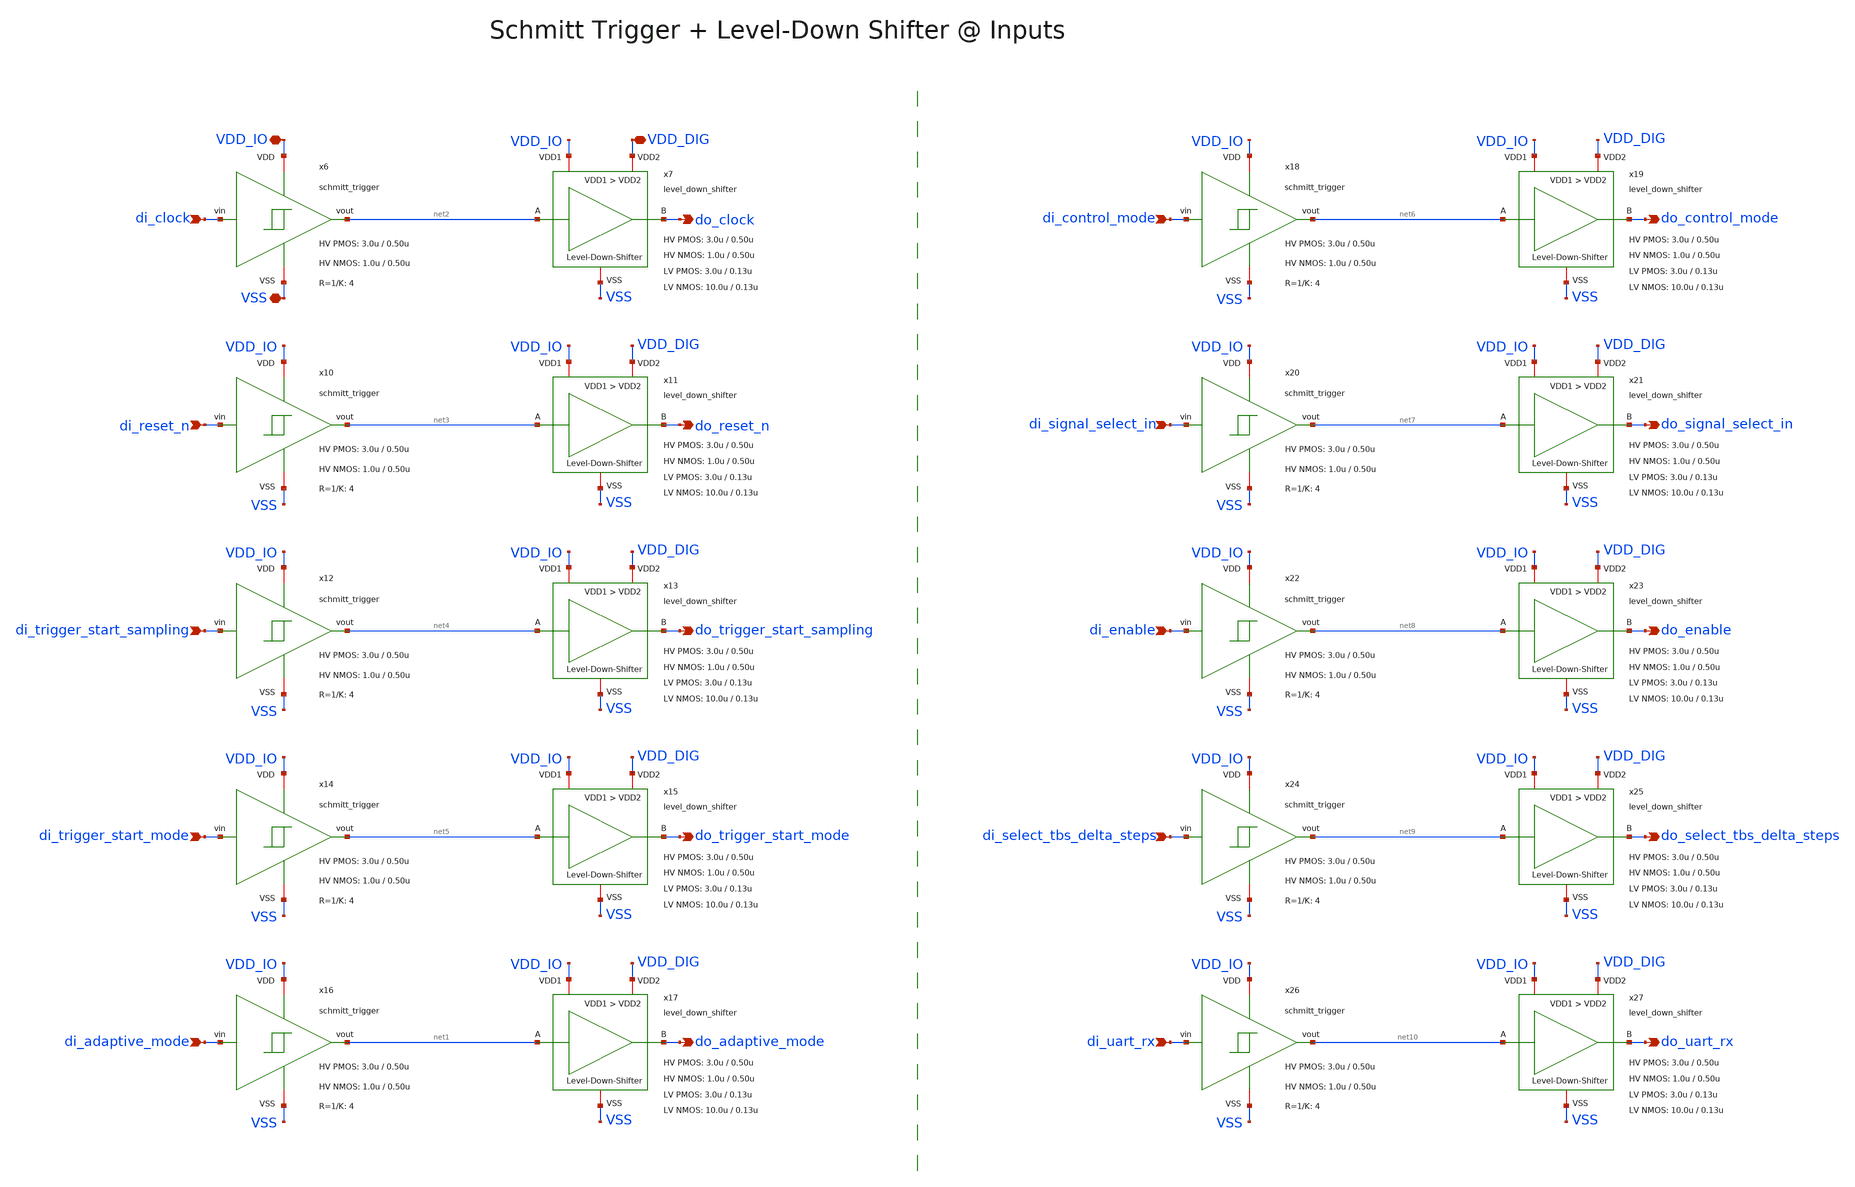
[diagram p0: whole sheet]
** sch_path: SG13G2_ATBS-ADC-main/xschem/top_level/auxiliary/input_hardware.sch
**.subckt input_hardware di_clock di_reset_n di_uart_rx di_trigger_start_sampling
*+ di_trigger_start_mode di_adaptive_mode di_control_mode di_signal_select_in di_enable di_select_tbs_delta_steps do_clock
*+ VDD_IO VDD_DIG do_trigger_start_sampling do_control_mode do_enable do_reset_n do_trigger_start_mode
*+ do_adaptive_mode do_signal_select_in do_select_tbs_delta_steps do_uart_rx VSS
*.ipin di_clock
*.ipin di_reset_n
*.ipin di_uart_rx
*.ipin di_trigger_start_sampling
*.ipin di_trigger_start_mode
*.ipin di_adaptive_mode
*.ipin di_control_mode
*.ipin di_signal_select_in
*.ipin di_enable
*.ipin di_select_tbs_delta_steps
*.opin do_clock
*.iopin VDD_IO
*.iopin VDD_DIG
*.opin do_trigger_start_sampling
*.opin do_control_mode
*.opin do_enable
*.opin do_reset_n
*.opin do_trigger_start_mode
*.opin do_adaptive_mode
*.opin do_signal_select_in
*.opin do_select_tbs_delta_steps
*.opin do_uart_rx
*.iopin VSS
x6 VDD_IO net2 di_clock VSS schmitt_trigger W_P_ST=3.0u L_P_ST=0.50u W_N_ST=1.0u L_N_ST=0.50u R=4
x7 VDD_DIG net2 do_clock VSS VDD_IO level_down_shifter W_P_HV=3.0u L_P_HV=0.50u W_N_HV=1.0u
+ L_N_HV=0.50u W_P_LV=3.0u L_P_LV=0.13u W_N_LV=10.0u L_N_LV=0.13u
x10 VDD_IO net3 di_reset_n VSS schmitt_trigger W_P_ST=3.0u L_P_ST=0.50u W_N_ST=1.0u L_N_ST=0.50u R=4
x11 VDD_DIG net3 do_reset_n VSS VDD_IO level_down_shifter W_P_HV=3.0u L_P_HV=0.50u W_N_HV=1.0u
+ L_N_HV=0.50u W_P_LV=3.0u L_P_LV=0.13u W_N_LV=10.0u L_N_LV=0.13u
x12 VDD_IO net4 di_trigger_start_sampling VSS schmitt_trigger W_P_ST=3.0u L_P_ST=0.50u W_N_ST=1.0u
+ L_N_ST=0.50u R=4
x13 VDD_DIG net4 do_trigger_start_sampling VSS VDD_IO level_down_shifter W_P_HV=3.0u L_P_HV=0.50u
+ W_N_HV=1.0u L_N_HV=0.50u W_P_LV=3.0u L_P_LV=0.13u W_N_LV=10.0u L_N_LV=0.13u
x14 VDD_IO net5 di_trigger_start_mode VSS schmitt_trigger W_P_ST=3.0u L_P_ST=0.50u W_N_ST=1.0u
+ L_N_ST=0.50u R=4
x15 VDD_DIG net5 do_trigger_start_mode VSS VDD_IO level_down_shifter W_P_HV=3.0u L_P_HV=0.50u
+ W_N_HV=1.0u L_N_HV=0.50u W_P_LV=3.0u L_P_LV=0.13u W_N_LV=10.0u L_N_LV=0.13u
x16 VDD_IO net1 di_adaptive_mode VSS schmitt_trigger W_P_ST=3.0u L_P_ST=0.50u W_N_ST=1.0u
+ L_N_ST=0.50u R=4
x17 VDD_DIG net1 do_adaptive_mode VSS VDD_IO level_down_shifter W_P_HV=3.0u L_P_HV=0.50u W_N_HV=1.0u
+ L_N_HV=0.50u W_P_LV=3.0u L_P_LV=0.13u W_N_LV=10.0u L_N_LV=0.13u
x18 VDD_IO net6 di_control_mode VSS schmitt_trigger W_P_ST=3.0u L_P_ST=0.50u W_N_ST=1.0u
+ L_N_ST=0.50u R=4
x19 VDD_DIG net6 do_control_mode VSS VDD_IO level_down_shifter W_P_HV=3.0u L_P_HV=0.50u W_N_HV=1.0u
+ L_N_HV=0.50u W_P_LV=3.0u L_P_LV=0.13u W_N_LV=10.0u L_N_LV=0.13u
x20 VDD_IO net7 di_signal_select_in VSS schmitt_trigger W_P_ST=3.0u L_P_ST=0.50u W_N_ST=1.0u
+ L_N_ST=0.50u R=4
x21 VDD_DIG net7 do_signal_select_in VSS VDD_IO level_down_shifter W_P_HV=3.0u L_P_HV=0.50u
+ W_N_HV=1.0u L_N_HV=0.50u W_P_LV=3.0u L_P_LV=0.13u W_N_LV=10.0u L_N_LV=0.13u
x22 VDD_IO net8 di_enable VSS schmitt_trigger W_P_ST=3.0u L_P_ST=0.50u W_N_ST=1.0u L_N_ST=0.50u R=4
x23 VDD_DIG net8 do_enable VSS VDD_IO level_down_shifter W_P_HV=3.0u L_P_HV=0.50u W_N_HV=1.0u
+ L_N_HV=0.50u W_P_LV=3.0u L_P_LV=0.13u W_N_LV=10.0u L_N_LV=0.13u
x24 VDD_IO net9 di_select_tbs_delta_steps VSS schmitt_trigger W_P_ST=3.0u L_P_ST=0.50u W_N_ST=1.0u
+ L_N_ST=0.50u R=4
x25 VDD_DIG net9 do_select_tbs_delta_steps VSS VDD_IO level_down_shifter W_P_HV=3.0u L_P_HV=0.50u
+ W_N_HV=1.0u L_N_HV=0.50u W_P_LV=3.0u L_P_LV=0.13u W_N_LV=10.0u L_N_LV=0.13u
x26 VDD_IO net10 di_uart_rx VSS schmitt_trigger W_P_ST=3.0u L_P_ST=0.50u W_N_ST=1.0u L_N_ST=0.50u
+ R=4
x27 VDD_DIG net10 do_uart_rx VSS VDD_IO level_down_shifter W_P_HV=3.0u L_P_HV=0.50u W_N_HV=1.0u
+ L_N_HV=0.50u W_P_LV=3.0u L_P_LV=0.13u W_N_LV=10.0u L_N_LV=0.13u
**.ends

* expanding   symbol:  schmitt_trigger/schmitt_trigger.sym # of pins=4
** sym_path: SG13G2_ATBS-ADC-main/xschem/schmitt_trigger/schmitt_trigger.sym
** sch_path: SG13G2_ATBS-ADC-main/xschem/schmitt_trigger/schmitt_trigger.sch
.subckt schmitt_trigger VDD vout vin VSS  W_P_ST=3.0u L_P_ST=0.50u W_N_ST=1.0u L_N_ST=0.50u R=4
*.iopin VDD
*.opin vout
*.iopin VSS
*.ipin vin
x1 VDD net2 vout VSS inverter_hv W_P=W_P_ST L_P=L_P_ST W_N=W_N_ST L_N=L_N_ST
XM5 net3 vin VDD VDD sg13_hv_pmos w=W_P_ST l=L_P_ST ng=1 m=1 mm_ok=1
XM4 net2 vin net3 VDD sg13_hv_pmos w=W_P_ST l=L_P_ST ng=1 m=1 mm_ok=1
XM6 VSS net2 net3 VDD sg13_hv_pmos w=R*W_P_ST l=L_P_ST ng=1 m=1 mm_ok=1
XM1 net1 vin VSS VSS sg13_hv_nmos w=W_N_ST l=L_N_ST ng=1 m=1 mm_ok=1
XM2 net2 vin net1 VSS sg13_hv_nmos w=W_N_ST l=L_N_ST ng=1 m=1 mm_ok=1
XM3 VDD net2 net1 VSS sg13_hv_nmos w=R*W_N_ST l=L_N_ST ng=1 m=1 mm_ok=1
.ends


* expanding   symbol:  level_shifter/level_down_shifter.sym # of pins=5
** sym_path: SG13G2_ATBS-ADC-main/xschem/level_shifter/level_down_shifter.sym
** sch_path: SG13G2_ATBS-ADC-main/xschem/level_shifter/level_down_shifter.sch
.subckt level_down_shifter VDD2 A B VSS VDD1  W_P_HV=3.0u L_P_HV=0.50u W_N_HV=1.0u L_N_HV=0.50u
+ W_P_LV=3.0u L_P_LV=0.13u W_N_LV=10.0u L_N_LV=0.13u
*.ipin A
*.iopin VDD1
*.iopin VSS
*.opin B
*.iopin VDD2
x3 VDD2 T B VSS inverter_lv W_P=W_P_LV L_P=L_P_LV W_N=0.1*W_N_LV L_N=L_N_LV
x1 VDD1 A A! VSS inverter_hv W_P=W_P_HV L_P=L_P_HV W_N=W_N_HV L_N=L_N_HV
x2 VDD1 A! net2 VSS inverter_hv W_P=W_P_HV L_P=L_P_HV W_N=W_N_HV L_N=L_N_HV
XM1 net1 A! VSS VSS sg13_lv_nmos w=W_N_LV l=L_N_LV ng=1 m=1 mm_ok=1
XM3 net1 T VDD2 VDD2 sg13_lv_pmos w=W_P_LV l=L_P_LV ng=1 m=1 mm_ok=1
XM2 T net2 VSS VSS sg13_lv_nmos w=W_N_LV l=L_N_LV ng=1 m=1 mm_ok=1
XM4 T net1 VDD2 VDD2 sg13_lv_pmos w=W_P_LV l=L_P_LV ng=1 m=1 mm_ok=1
.ends


* expanding   symbol:  inverter/inverter_hv.sym # of pins=4
** sym_path: SG13G2_ATBS-ADC-main/xschem/inverter/inverter_hv.sym
** sch_path: SG13G2_ATBS-ADC-main/xschem/inverter/inverter_hv.sch
.subckt inverter_hv VDD vin vout VSS  W_P=3.0u L_P=0.50u W_N=1.0u L_N=0.50u
*.ipin vin
*.iopin VDD
*.iopin VSS
*.opin vout
XM1 vout vin VDD VDD sg13_hv_pmos w=W_P l=L_P ng=1 m=1 mm_ok=1
XM2 vout vin VSS VSS sg13_hv_nmos w=W_N l=L_N ng=1 m=1 mm_ok=1
.ends


* expanding   symbol:  inverter/inverter_lv.sym # of pins=4
** sym_path: SG13G2_ATBS-ADC-main/xschem/inverter/inverter_lv.sym
** sch_path: SG13G2_ATBS-ADC-main/xschem/inverter/inverter_lv.sch
.subckt inverter_lv VDD vin vout VSS  W_P=3.0u L_P=0.13u W_N=1.0u L_N=0.13u
*.ipin vin
*.iopin VDD
*.iopin VSS
*.opin vout
XM1 vout vin VDD VDD sg13_lv_pmos w=W_P l=L_P ng=1 m=1 mm_ok=1
XM2 vout vin VSS VSS sg13_lv_nmos w=W_N l=L_N ng=1 m=1 mm_ok=1
.ends

.end
